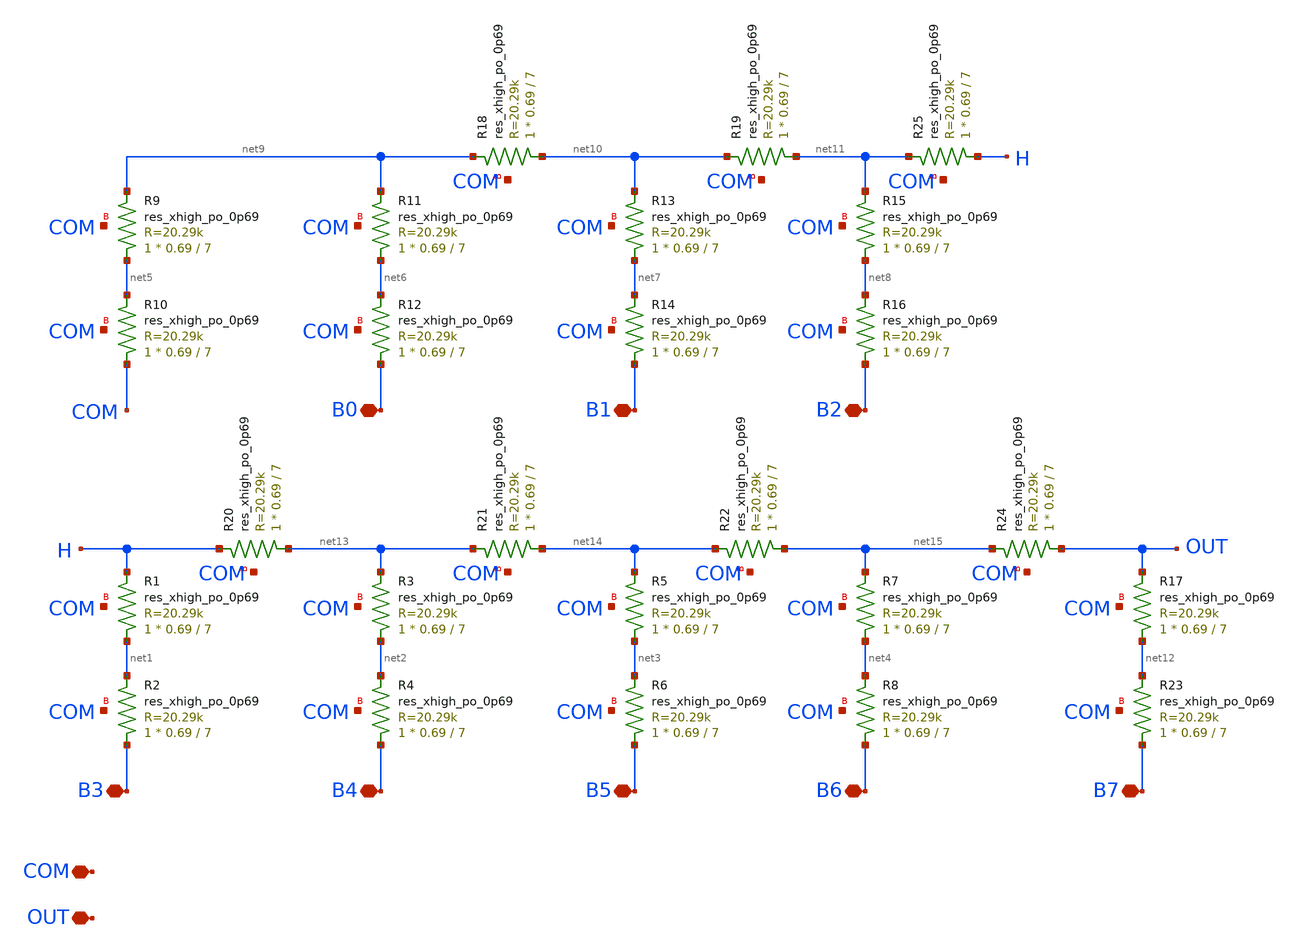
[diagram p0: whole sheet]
** sch_path: xschem/R2R_20k.sch
**.subckt R2R_20k COM B0 B1 OUT B2 B3 B4 B5 B6 B7
*.iopin COM
*.iopin B0
*.iopin B1
*.iopin OUT
*.iopin B2
*.iopin B3
*.iopin B4
*.iopin B5
*.iopin B6
*.iopin B7
XR1 net1 H COM sky130_fd_pr__res_xhigh_po_0p69 L=7 mult=1 m=1
XR2 B3 net1 COM sky130_fd_pr__res_xhigh_po_0p69 L=7 mult=1 m=1
XR3 net2 net13 COM sky130_fd_pr__res_xhigh_po_0p69 L=7 mult=1 m=1
XR4 B4 net2 COM sky130_fd_pr__res_xhigh_po_0p69 L=7 mult=1 m=1
XR5 net3 net14 COM sky130_fd_pr__res_xhigh_po_0p69 L=7 mult=1 m=1
XR6 B5 net3 COM sky130_fd_pr__res_xhigh_po_0p69 L=7 mult=1 m=1
XR7 net4 net15 COM sky130_fd_pr__res_xhigh_po_0p69 L=7 mult=1 m=1
XR8 B6 net4 COM sky130_fd_pr__res_xhigh_po_0p69 L=7 mult=1 m=1
XR9 net5 net9 COM sky130_fd_pr__res_xhigh_po_0p69 L=7 mult=1 m=1
XR10 COM net5 COM sky130_fd_pr__res_xhigh_po_0p69 L=7 mult=1 m=1
XR11 net6 net9 COM sky130_fd_pr__res_xhigh_po_0p69 L=7 mult=1 m=1
XR12 B0 net6 COM sky130_fd_pr__res_xhigh_po_0p69 L=7 mult=1 m=1
XR13 net7 net10 COM sky130_fd_pr__res_xhigh_po_0p69 L=7 mult=1 m=1
XR14 B1 net7 COM sky130_fd_pr__res_xhigh_po_0p69 L=7 mult=1 m=1
XR15 net8 net11 COM sky130_fd_pr__res_xhigh_po_0p69 L=7 mult=1 m=1
XR16 B2 net8 COM sky130_fd_pr__res_xhigh_po_0p69 L=7 mult=1 m=1
XR18 net10 net9 COM sky130_fd_pr__res_xhigh_po_0p69 L=7 mult=1 m=1
XR19 net11 net10 COM sky130_fd_pr__res_xhigh_po_0p69 L=7 mult=1 m=1
XR20 net13 H COM sky130_fd_pr__res_xhigh_po_0p69 L=7 mult=1 m=1
XR21 net14 net13 COM sky130_fd_pr__res_xhigh_po_0p69 L=7 mult=1 m=1
XR22 net15 net14 COM sky130_fd_pr__res_xhigh_po_0p69 L=7 mult=1 m=1
XR17 net12 OUT COM sky130_fd_pr__res_xhigh_po_0p69 L=7 mult=1 m=1
XR23 B7 net12 COM sky130_fd_pr__res_xhigh_po_0p69 L=7 mult=1 m=1
XR24 OUT net15 COM sky130_fd_pr__res_xhigh_po_0p69 L=7 mult=1 m=1
XR25 H net11 COM sky130_fd_pr__res_xhigh_po_0p69 L=7 mult=1 m=1
**.ends
.end
